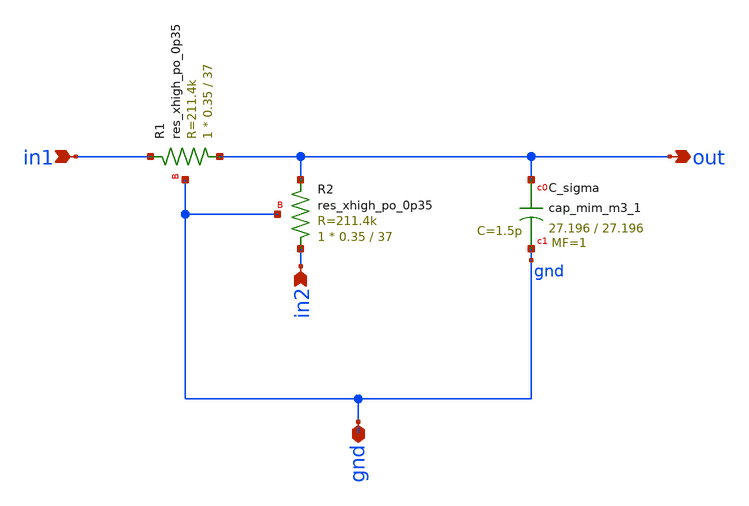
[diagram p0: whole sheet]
** sch_path: mag/sigma-delta_modulator/xschem/sum-integ.sch
* Copyright 2020 Stefan Frederik Schippers
* Licensed under the Apache License, Version 2.0 (the "License");
* you may not use this file except in compliance with the License.
* You may obtain a copy of the License at
* https://www.apache.org/licenses/LICENSE-2.0
* Unless required by applicable law or agreed to in writing, software
* distributed under the License is distributed on an "AS IS" BASIS,
* WITHOUT WARRANTIES OR CONDITIONS OF ANY KIND, either express or implied.
* See the License for the specific language governing permissions and
* limitations under the License.
**.subckt sum-integ in1 gnd out in2
*.ipin in1
*.iopin gnd
*.opin out
*.ipin in2
XC_sigma out gnd sky130_fd_pr__cap_mim_m3_1 W=27.196 L=27.196 MF=1 m=1
XR1 out in1 gnd sky130_fd_pr__res_xhigh_po_0p35 L=37 mult=1 m=1
XR2 in2 out gnd sky130_fd_pr__res_xhigh_po_0p35 L=37 mult=1 m=1
**** begin user architecture code




**** end user architecture code
**.ends
.end
